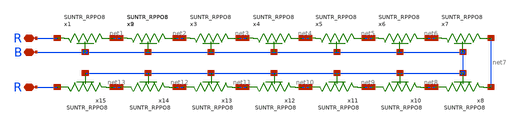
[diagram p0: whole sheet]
** sch_path: design/CNR_GR05_SKY130NM/M_OHM.sch
**.subckt M_OHM R R B
*.iopin R
*.iopin R
*.iopin B
x1 net1 R B SUNTR_RPPO8 xoffset=0 yoffset=0 angle=0 M=1
x2 net2 net1 B SUNTR_RPPO8 xoffset=0 yoffset=0 angle=0 M=1
x3 net3 net2 B SUNTR_RPPO8 xoffset=0 yoffset=0 angle=0 M=1
x4 net4 net3 B SUNTR_RPPO8 xoffset=0 yoffset=0 angle=0 M=1
x5 net5 net4 B SUNTR_RPPO8 xoffset=0 yoffset=0 angle=0 M=1
x6 net6 net5 B SUNTR_RPPO8 xoffset=0 yoffset=0 angle=0 M=1
x7 net7 net6 B SUNTR_RPPO8 xoffset=0 yoffset=0 angle=0 M=1
x8 net8 net7 B SUNTR_RPPO8 xoffset=0 yoffset=0 angle=0 M=1
x9 net2 net1 B SUNTR_RPPO8 xoffset=0 yoffset=0 angle=0 M=1
x10 net9 net8 B SUNTR_RPPO8 xoffset=0 yoffset=0 angle=0 M=1
x11 net10 net9 B SUNTR_RPPO8 xoffset=0 yoffset=0 angle=0 M=1
x12 net11 net10 B SUNTR_RPPO8 xoffset=0 yoffset=0 angle=0 M=1
x13 net12 net11 B SUNTR_RPPO8 xoffset=0 yoffset=0 angle=0 M=1
x14 net13 net12 B SUNTR_RPPO8 xoffset=0 yoffset=0 angle=0 M=1
x15 R net13 B SUNTR_RPPO8 xoffset=0 yoffset=0 angle=0 M=1
**.ends

* expanding   symbol:  SUN_TR_SKY130NM/SUNTR_RPPO8.sym # of pins=3
** sym_path: SUN_TR_SKY130NM/SUNTR_RPPO8.sym
** sch_path: SUN_TR_SKY130NM/SUNTR_RPPO8.sch
.subckt SUNTR_RPPO8 N P B  xoffset=0 yoffset=0 angle=0 M=1
*.iopin P
*.iopin N
*.iopin B
XXA1 N P B SUNTR_RES8 xoffset=0 yoffset=0 angle=0
.ends


* expanding   symbol:  SUN_TR_SKY130NM/SUNTR_RES8.sym # of pins=3
** sym_path: SUN_TR_SKY130NM/SUNTR_RES8.sym
** sch_path: SUN_TR_SKY130NM/SUNTR_RES8.sch
.subckt SUNTR_RES8 N P B  xoffset=0 yoffset=0 angle=0
*.iopin N
*.iopin P
*.iopin B
XR1_0 INT_0 N B sky130_fd_pr__res_high_po W=0.72 L=8.8 mult=1 m=1
XR1_1 INT_1 INT_0 B sky130_fd_pr__res_high_po W=0.72 L=8.8 mult=1 m=1
XR1_2 INT_2 INT_1 B sky130_fd_pr__res_high_po W=0.72 L=8.8 mult=1 m=1
XR1_3 INT_3 INT_2 B sky130_fd_pr__res_high_po W=0.72 L=8.8 mult=1 m=1
XR1_4 INT_4 INT_3 B sky130_fd_pr__res_high_po W=0.72 L=8.8 mult=1 m=1
XR1_5 INT_5 INT_4 B sky130_fd_pr__res_high_po W=0.72 L=8.8 mult=1 m=1
XR1_6 INT_6 INT_5 B sky130_fd_pr__res_high_po W=0.72 L=8.8 mult=1 m=1
XR1_7 P INT_6 B sky130_fd_pr__res_high_po W=0.72 L=8.8 mult=1 m=1
.ends

.end
